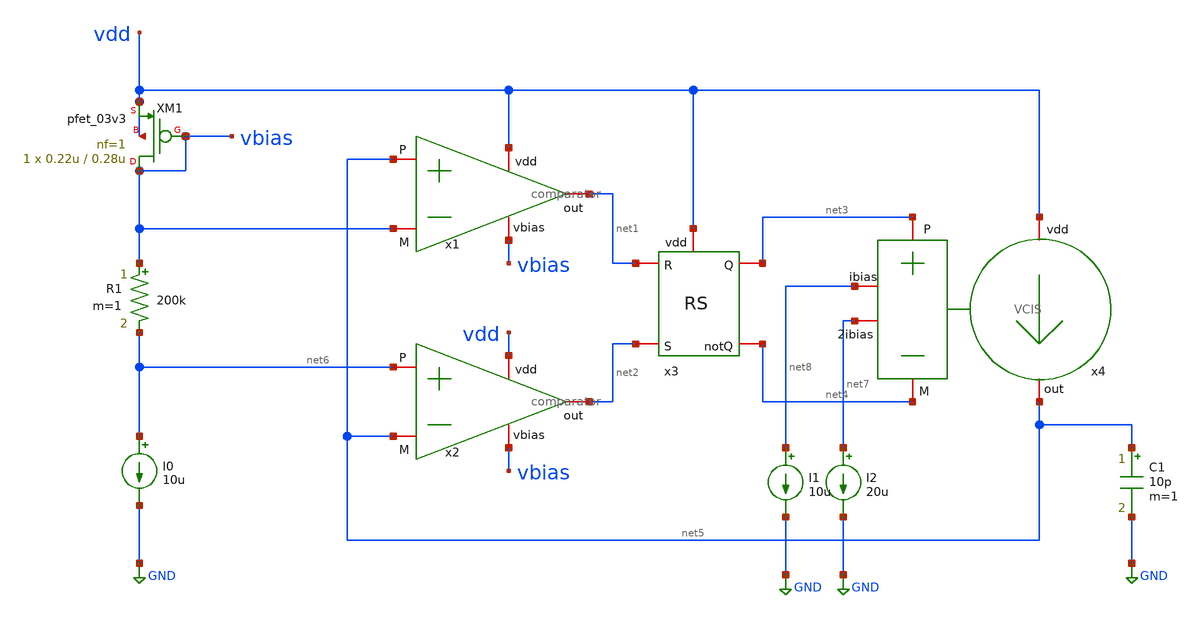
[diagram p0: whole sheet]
** sch_path: Clock_Reference/xschem/untitled.sch
**.subckt untitled
x1 vdd vbias net5 vbias net1 comparator
x2 vdd vbias net6 net5 net2 comparator
x3 vdd net1 net2 net3 net4 RS
x4 vdd net5 net3 net4 net8 net7 VCIS
C1 net5 GND 10p m=1
R1 vbias net6 200k m=1
XM1 vbias vbias vdd vdd pfet_03v3 L=0.28u W=0.22u nf=1 ad='int((nf+1)/2) * W/nf * 0.18u' as='int((nf+2)/2) * W/nf * 0.18u'
+ pd='2*int((nf+1)/2) * (W/nf + 0.18u)' ps='2*int((nf+2)/2) * (W/nf + 0.18u)' nrd='0.18u / W' nrs='0.18u / W'
+ sa=0 sb=0 sd=0 m=1
I0 net6 GND 10u
I1 net8 GND 10u
I2 net7 GND 20u
**.ends
.GLOBAL GND
.end
